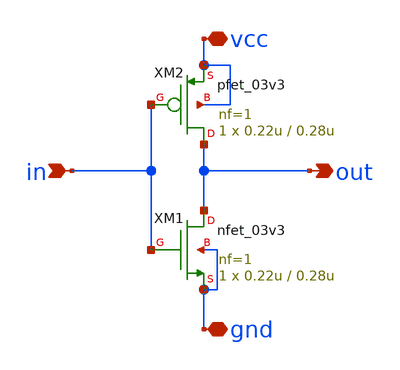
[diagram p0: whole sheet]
** sch_path: designs/schematics/mux2x1/inv.sch
**.subckt inv in out vcc gnd
*.ipin in
*.opin out
*.iopin vcc
*.iopin gnd
XM2 out in vcc vcc pfet_03v3 L=0.28u W=0.22u nf=1 ad='int((nf+1)/2) * W/nf * 0.18u' as='int((nf+2)/2) * W/nf * 0.18u'
+ pd='2*int((nf+1)/2) * (W/nf + 0.18u)' ps='2*int((nf+2)/2) * (W/nf + 0.18u)' nrd='0.18u / W' nrs='0.18u / W'
+ sa=0 sb=0 sd=0 m=1
XM1 out in gnd gnd nfet_03v3 L=0.28u W=0.22u nf=1 ad='int((nf+1)/2) * W/nf * 0.18u' as='int((nf+2)/2) * W/nf * 0.18u'
+ pd='2*int((nf+1)/2) * (W/nf + 0.18u)' ps='2*int((nf+2)/2) * (W/nf + 0.18u)' nrd='0.18u / W' nrs='0.18u / W'
+ sa=0 sb=0 sd=0 m=1
**.ends
.end
